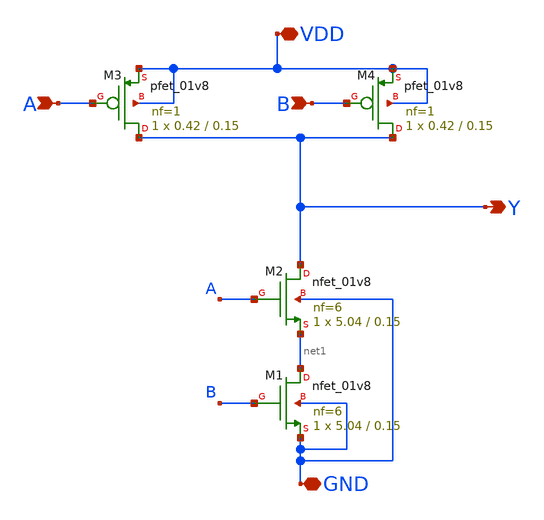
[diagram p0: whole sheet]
** sch_path: cells/NAND2X1/schematic/nand2x1.sch
**.subckt nand2x1 A B VDD GND Y
*.ipin A
*.ipin B
*.iopin VDD
*.iopin GND
*.opin Y
XM2 Y A net1 GND sky130_fd_pr__nfet_01v8 L=0.15 W=5.04 nf=6 ad='int((6 + 1)/2) * 5.04 / 6 * 0.29' as='int((6 + 2)/2) * 5.04 / 6 * 0.29'
+ pd='2*int((6 + 1)/2) * (5.04 / 6 + 0.29)' ps='2*int((6 + 2)/2) * (5.04 / 6 + 0.29)' nrd='0.29 / 5.04 '
+ nrs='0.29 / 5.04 ' sa=0 sb=0 sd=0 mult=1 m=1
XM3 Y A VDD VDD sky130_fd_pr__pfet_01v8 L=0.15 W=0.42 nf=1 ad='int((1 + 1)/2) * 0.42 / 1 * 0.29' as='int((1 + 2)/2) * 0.42 / 1 * 0.29'
+ pd='2*int((1 + 1)/2) * (0.42 / 1 + 0.29)' ps='2*int((1 + 2)/2) * (0.42 / 1 + 0.29)' nrd='0.29 / 0.42 '
+ nrs='0.29 / 0.42 ' sa=0 sb=0 sd=0 mult=1 m=1
XM4 Y B VDD VDD sky130_fd_pr__pfet_01v8 L=0.15 W=0.42 nf=1 ad='int((1 + 1)/2) * 0.42 / 1 * 0.29' as='int((1 + 2)/2) * 0.42 / 1 * 0.29'
+ pd='2*int((1 + 1)/2) * (0.42 / 1 + 0.29)' ps='2*int((1 + 2)/2) * (0.42 / 1 + 0.29)' nrd='0.29 / 0.42 '
+ nrs='0.29 / 0.42 ' sa=0 sb=0 sd=0 mult=1 m=1
XM1 net1 B GND GND sky130_fd_pr__nfet_01v8 L=0.15 W=5.04 nf=6 ad='int((6 + 1)/2) * 5.04 / 6 * 0.29' as='int((6 + 2)/2) * 5.04 / 6 * 0.29'
+ pd='2*int((6 + 1)/2) * (5.04 / 6 + 0.29)' ps='2*int((6 + 2)/2) * (5.04 / 6 + 0.29)' nrd='0.29 / 5.04 '
+ nrs='0.29 / 5.04 ' sa=0 sb=0 sd=0 mult=1 m=1
**.ends
.end
